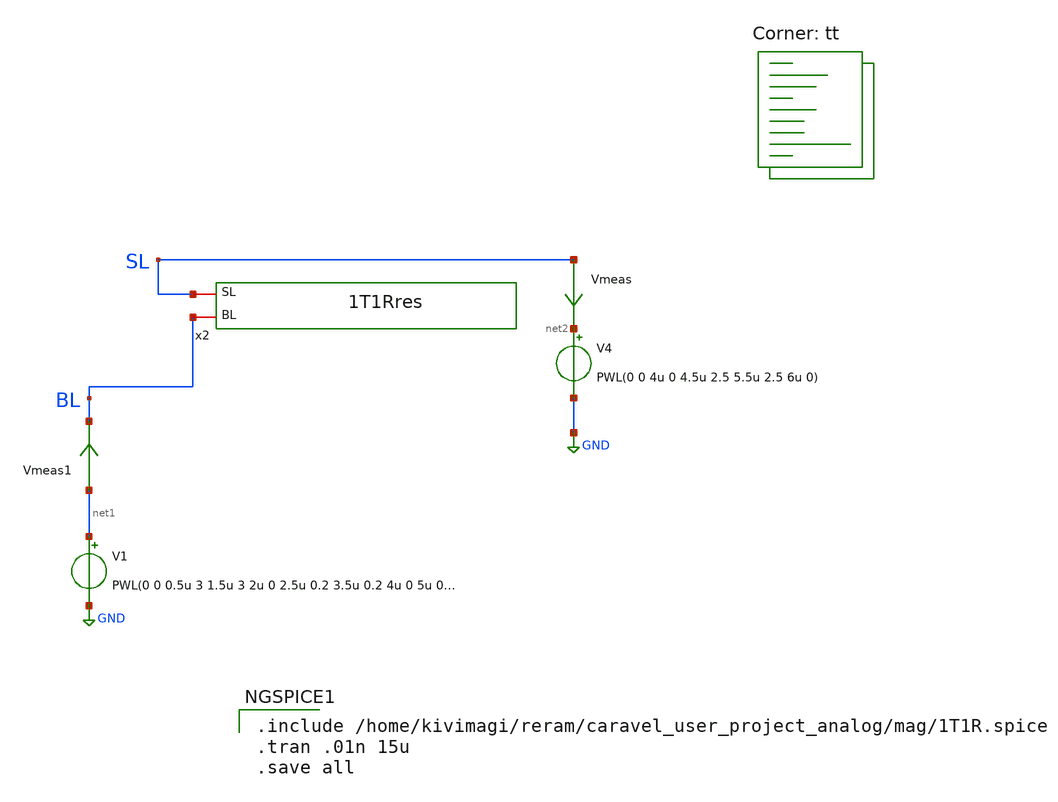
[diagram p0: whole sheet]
** sch_path: xschem/Crossbar/1t1rresTB.sch
**.subckt 1t1rresTB
Vmeas SL net2 0
.save i(vmeas)
Vmeas1 net1 BL 0
.save i(vmeas1)
V1 net1 GND PWL(0 0 0.5u 3 1.5u 3 2u 0 2.5u 0.2 3.5u 0.2 4u 0 5u 0 5.5u 0 6u 0 7u 0.2)
V4 net2 GND PWL(0 0 4u 0 4.5u 2.5 5.5u 2.5 6u 0)
x2 BL SL 1T1Rres
**** begin user architecture code
.lib $::SKYWATER_MODELS/sky130.lib.spice tt

.include /home/kivimagi/reram/caravel_user_project_analog/mag/1T1R.spice
.tran .01n 15u
.save all


**** end user architecture code
**.ends
.GLOBAL GND
.end
